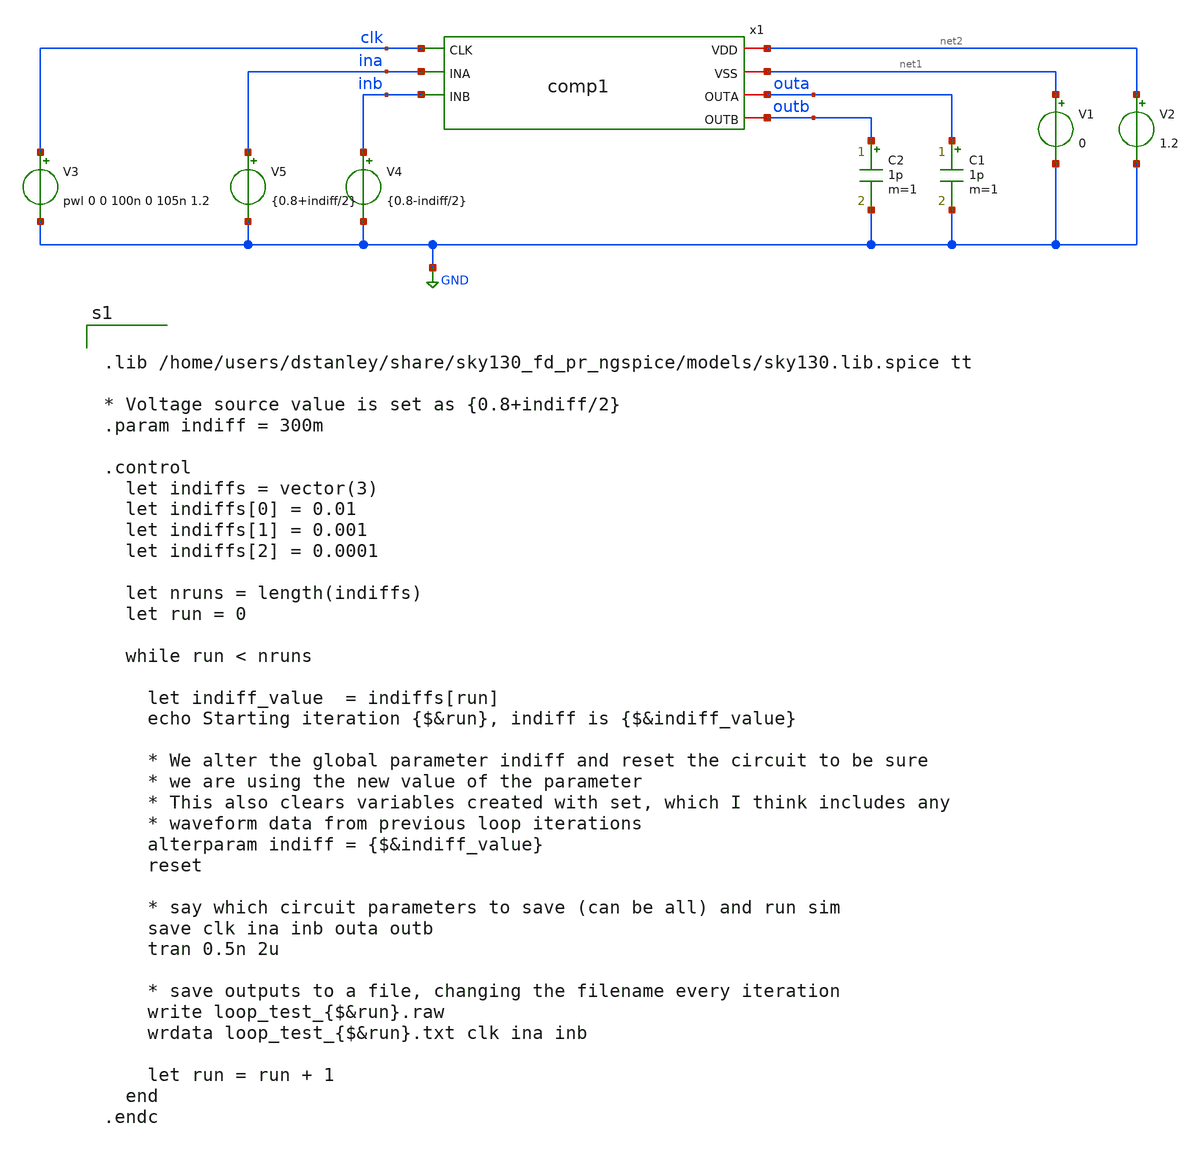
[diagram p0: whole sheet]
** sch_path: comp1_loop_test.sch
**.subckt comp1_loop_test
x1 net2 net1 clk ina inb outa outb comp1
V1 net1 GND 0
V2 net2 GND 1.2
C1 outa GND 1p m=1
C2 outb GND 1p m=1
V3 clk GND pwl 0 0 100n 0 105n 1.2
V4 inb GND {0.8-indiff/2}
V5 ina GND {0.8+indiff/2}
**** begin user architecture code


.lib /home/users/dstanley/share/sky130_fd_pr_ngspice/models/sky130.lib.spice tt

* Voltage source value is set as {0.8+indiff/2}
.param indiff = 300m

.control
  let indiffs = vector(3)
  let indiffs[0] = 0.01
  let indiffs[1] = 0.001
  let indiffs[2] = 0.0001

  let nruns = length(indiffs)
  let run = 0

  while run < nruns

    let indiff_value  = indiffs[run]
    echo Starting iteration {$&run}, indiff is {$&indiff_value}

    * We alter the global parameter indiff and reset the circuit to be sure
    * we are using the new value of the parameter
    * This also clears variables created with set, which I think includes any
    * waveform data from previous loop iterations
    alterparam indiff = {$&indiff_value}
    reset

    * say which circuit parameters to save (can be all) and run sim
    save clk ina inb outa outb
    tran 0.5n 2u

    * save outputs to a file, changing the filename every iteration
    write loop_test_{$&run}.raw
    wrdata loop_test_{$&run}.txt clk ina inb

    let run = run + 1
  end
.endc


**** end user architecture code
**.ends

* expanding   symbol:  /home/users/dstanley/EE272B/xschem_tests/comp1.sym # of pins=7
** sym_path: comp1.sym
** sch_path: comp1.sch
.subckt comp1 VDD VSS CLK INA INB OUTA OUTB
*.iopin VSS
*.iopin VDD
*.iopin OUTB
*.iopin OUTA
*.ipin INB
*.ipin INA
*.ipin CLK
XM1 net2 CLK VSS VSS sky130_fd_pr__nfet_01v8 L=0.15 W=1 nf=1 ad='int((nf+1)/2) * W/nf * 0.29' as='int((nf+2)/2) * W/nf * 0.29'
+ pd='2*int((nf+1)/2) * (W/nf + 0.29)' ps='2*int((nf+2)/2) * (W/nf + 0.29)' nrd='0.29 / W' nrs='0.29 / W'
+ sa=0 sb=0 sd=0 mult=1 m=1
XM2 net1 INA net2 VSS sky130_fd_pr__nfet_01v8 L=0.15 W=1 nf=1 ad='int((nf+1)/2) * W/nf * 0.29' as='int((nf+2)/2) * W/nf * 0.29'
+ pd='2*int((nf+1)/2) * (W/nf + 0.29)' ps='2*int((nf+2)/2) * (W/nf + 0.29)' nrd='0.29 / W' nrs='0.29 / W'
+ sa=0 sb=0 sd=0 mult=1 m=1
XM4 OUTB OUTA net1 VSS sky130_fd_pr__nfet_01v8 L=0.15 W=1 nf=1 ad='int((nf+1)/2) * W/nf * 0.29' as='int((nf+2)/2) * W/nf * 0.29'
+ pd='2*int((nf+1)/2) * (W/nf + 0.29)' ps='2*int((nf+2)/2) * (W/nf + 0.29)' nrd='0.29 / W' nrs='0.29 / W'
+ sa=0 sb=0 sd=0 mult=1 m=1
XM5 OUTB OUTA VDD VDD sky130_fd_pr__pfet_01v8 L=0.15 W=1 nf=1 ad='int((nf+1)/2) * W/nf * 0.29' as='int((nf+2)/2) * W/nf * 0.29'
+ pd='2*int((nf+1)/2) * (W/nf + 0.29)' ps='2*int((nf+2)/2) * (W/nf + 0.29)' nrd='0.29 / W' nrs='0.29 / W'
+ sa=0 sb=0 sd=0 mult=1 m=1
XM6 OUTB CLK VDD VDD sky130_fd_pr__pfet_01v8 L=0.15 W=1 nf=1 ad='int((nf+1)/2) * W/nf * 0.29' as='int((nf+2)/2) * W/nf * 0.29'
+ pd='2*int((nf+1)/2) * (W/nf + 0.29)' ps='2*int((nf+2)/2) * (W/nf + 0.29)' nrd='0.29 / W' nrs='0.29 / W'
+ sa=0 sb=0 sd=0 mult=1 m=1
XM3 net3 INB net2 VSS sky130_fd_pr__nfet_01v8 L=0.15 W=1 nf=1 ad='int((nf+1)/2) * W/nf * 0.29' as='int((nf+2)/2) * W/nf * 0.29'
+ pd='2*int((nf+1)/2) * (W/nf + 0.29)' ps='2*int((nf+2)/2) * (W/nf + 0.29)' nrd='0.29 / W' nrs='0.29 / W'
+ sa=0 sb=0 sd=0 mult=1 m=1
XM7 OUTA OUTB net3 VSS sky130_fd_pr__nfet_01v8 L=0.15 W=1 nf=1 ad='int((nf+1)/2) * W/nf * 0.29' as='int((nf+2)/2) * W/nf * 0.29'
+ pd='2*int((nf+1)/2) * (W/nf + 0.29)' ps='2*int((nf+2)/2) * (W/nf + 0.29)' nrd='0.29 / W' nrs='0.29 / W'
+ sa=0 sb=0 sd=0 mult=1 m=1
XM8 OUTA OUTB VDD VDD sky130_fd_pr__pfet_01v8 L=0.15 W=1 nf=1 ad='int((nf+1)/2) * W/nf * 0.29' as='int((nf+2)/2) * W/nf * 0.29'
+ pd='2*int((nf+1)/2) * (W/nf + 0.29)' ps='2*int((nf+2)/2) * (W/nf + 0.29)' nrd='0.29 / W' nrs='0.29 / W'
+ sa=0 sb=0 sd=0 mult=1 m=1
XM9 OUTA CLK VDD VDD sky130_fd_pr__pfet_01v8 L=0.15 W=1 nf=1 ad='int((nf+1)/2) * W/nf * 0.29' as='int((nf+2)/2) * W/nf * 0.29'
+ pd='2*int((nf+1)/2) * (W/nf + 0.29)' ps='2*int((nf+2)/2) * (W/nf + 0.29)' nrd='0.29 / W' nrs='0.29 / W'
+ sa=0 sb=0 sd=0 mult=1 m=1
.ends

.GLOBAL GND
.end
